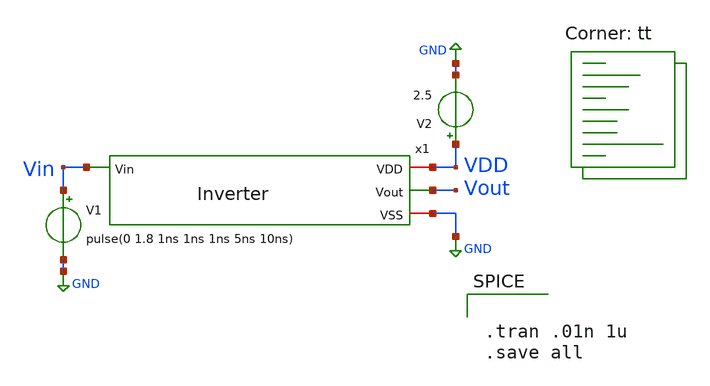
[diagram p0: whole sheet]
** sch_path: xschem/Testbenches/InverterTB.sch
**.subckt InverterTB
V1 Vin GND pulse(0 1.8 1ns 1ns 1ns 5ns 10ns)
V2 VDD GND 2.5
x1 VDD Vin Vout GND Inverter
**** begin user architecture code


.tran .01n 1u
.save all

.lib $::SKYWATER_MODELS/sky130.lib.spice tt
**** end user architecture code
**.ends

* expanding   symbol:  Inverter.sym # of pins=4
** sym_path: xschem/Inverter.sym
** sch_path: xschem/Inverter.sch
.subckt Inverter VDD Vin Vout VSS
*.ipin Vin
*.iopin VDD
*.iopin VSS
*.opin Vout
XM1 Vout Vin VSS VSS sky130_fd_pr__nfet_g5v0d10v5 L=0.5 W=0.75 nf=1 ad='int((nf+1)/2) * W/nf * 0.29'
+ as='int((nf+2)/2) * W/nf * 0.29' pd='2*int((nf+1)/2) * (W/nf + 0.29)' ps='2*int((nf+2)/2) * (W/nf + 0.29)'
+ nrd='0.29 / W' nrs='0.29 / W' sa=0 sb=0 sd=0 mult=1 m=1
XM2 Vout Vin VDD VDD sky130_fd_pr__pfet_g5v0d10v5 L=0.5 W=1.5 nf=1 ad='int((nf+1)/2) * W/nf * 0.29' as='int((nf+2)/2) * W/nf * 0.29'
+ pd='2*int((nf+1)/2) * (W/nf + 0.29)' ps='2*int((nf+2)/2) * (W/nf + 0.29)' nrd='0.29 / W' nrs='0.29 / W'
+ sa=0 sb=0 sd=0 mult=1 m=1
.ends

.GLOBAL GND
.end
